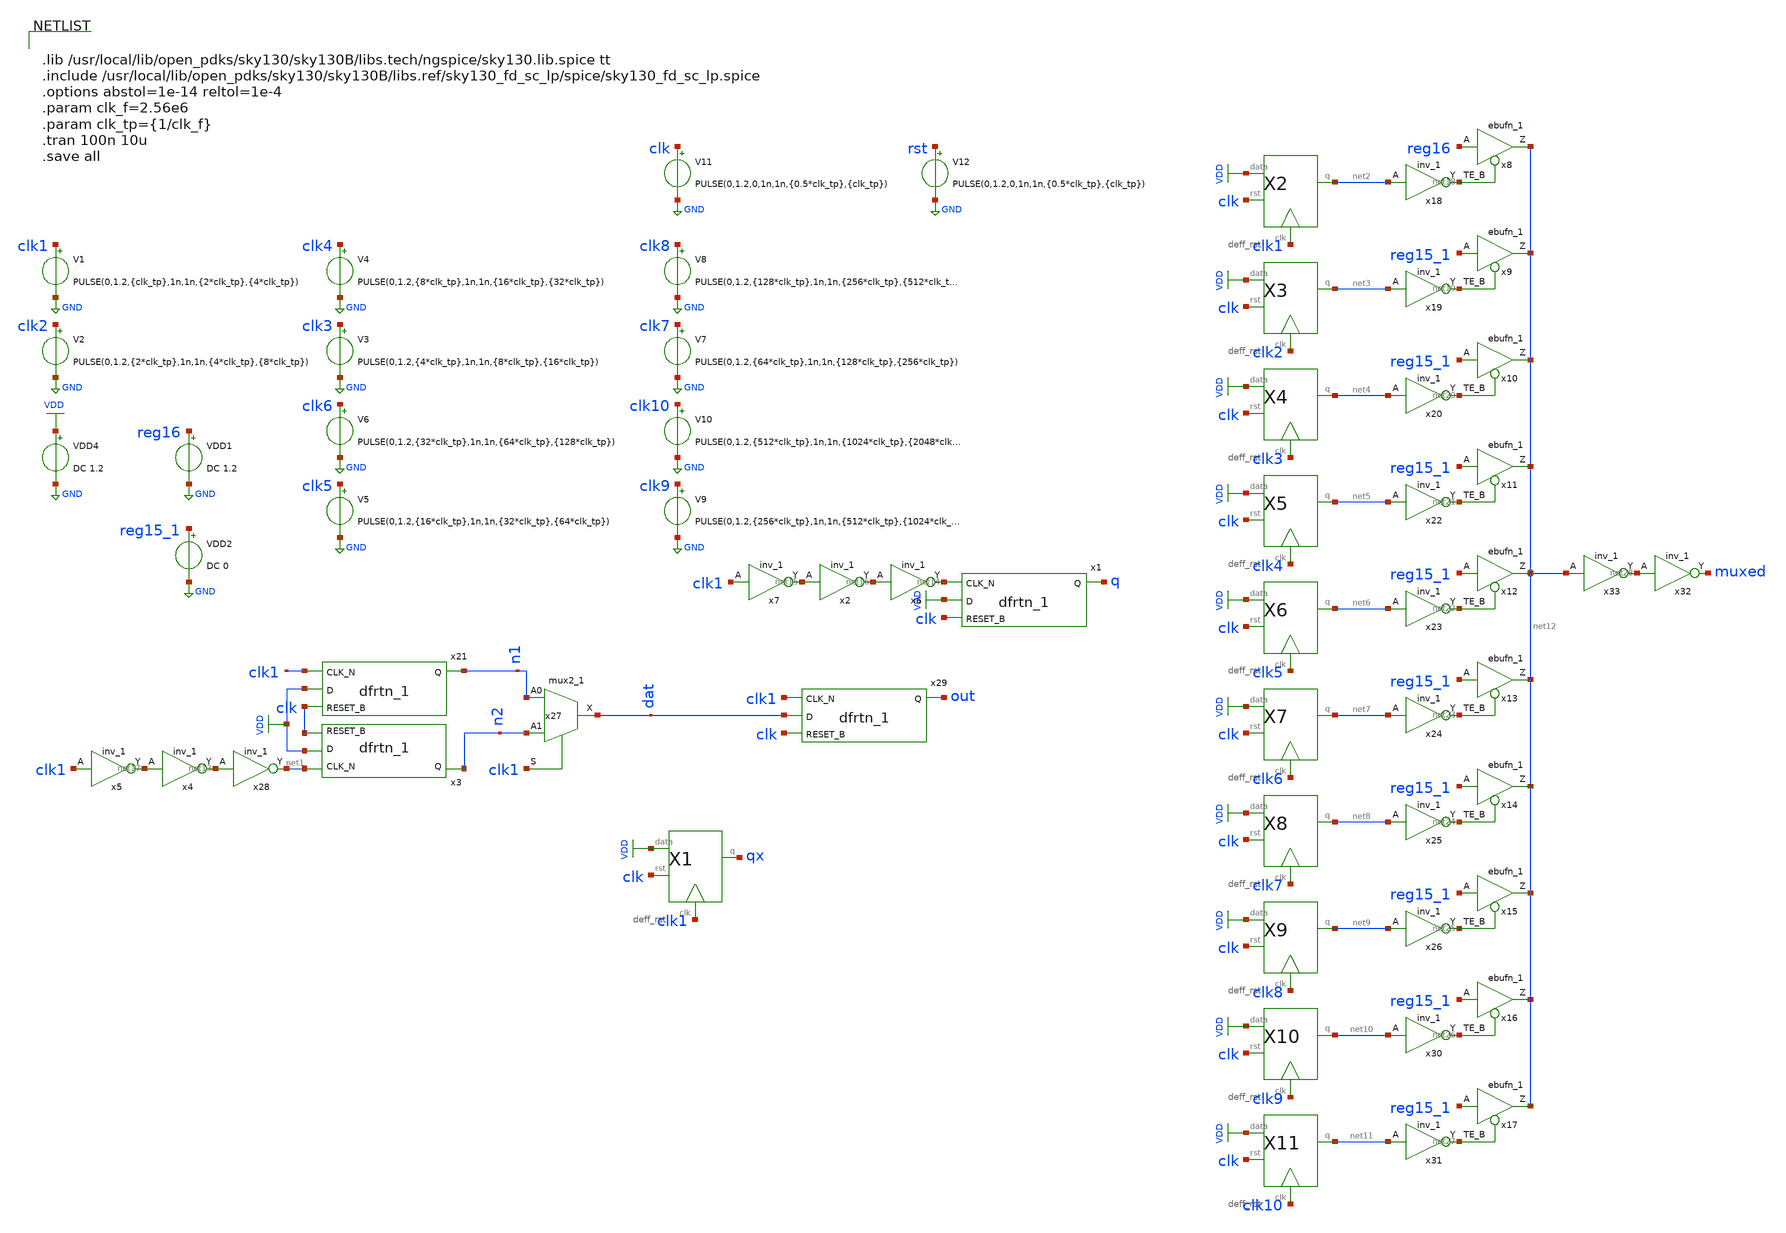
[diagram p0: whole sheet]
** sch_path: xschem/tryandtest/grayselection.sch
**.subckt grayselection
V1 clk1 GND PULSE(0,1.2,{clk_tp},1n,1n,{2*clk_tp},{4*clk_tp})
VDD4 VDD GND DC 1.2
V2 clk2 GND PULSE(0,1.2,{2*clk_tp},1n,1n,{4*clk_tp},{8*clk_tp})
V3 clk3 GND PULSE(0,1.2,{4*clk_tp},1n,1n,{8*clk_tp},{16*clk_tp})
V4 clk4 GND PULSE(0,1.2,{8*clk_tp},1n,1n,{16*clk_tp},{32*clk_tp})
V5 clk5 GND PULSE(0,1.2,{16*clk_tp},1n,1n,{32*clk_tp},{64*clk_tp})
V6 clk6 GND PULSE(0,1.2,{32*clk_tp},1n,1n,{64*clk_tp},{128*clk_tp})
V7 clk7 GND PULSE(0,1.2,{64*clk_tp},1n,1n,{128*clk_tp},{256*clk_tp})
V8 clk8 GND PULSE(0,1.2,{128*clk_tp},1n,1n,{256*clk_tp},{512*clk_tp})
V9 clk9 GND PULSE(0,1.2,{256*clk_tp},1n,1n,{512*clk_tp},{1024*clk_tp})
V10 clk10 GND PULSE(0,1.2,{512*clk_tp},1n,1n,{1024*clk_tp},{2048*clk_tp})
VDD1 reg16 GND DC 1.2
VDD2 reg15_1 GND DC 0
V11 clk GND PULSE(0,1.2,0,1n,1n,{0.5*clk_tp},{clk_tp})
x27 n1 n2 clk1 GND GND VDD VDD dat sky130_fd_sc_lp__mux2_1
x28 net13 GND GND VDD VDD net1 sky130_fd_sc_lp__inv_1
x29 clk1 dat clk GND GND VDD VDD out sky130_fd_sc_lp__dfrtn_1
x21 clk1 VDD clk GND GND VDD VDD n1 sky130_fd_sc_lp__dfrtn_1
x1 net14 VDD clk GND GND VDD VDD q sky130_fd_sc_lp__dfrtn_1
x2 net15 GND GND VDD VDD net16 sky130_fd_sc_lp__inv_1
x6 net16 GND GND VDD VDD net14 sky130_fd_sc_lp__inv_1
x7 clk1 GND GND VDD VDD net15 sky130_fd_sc_lp__inv_1
x3 net1 VDD clk GND GND VDD VDD n2 sky130_fd_sc_lp__dfrtn_1
x4 net17 GND GND VDD VDD net13 sky130_fd_sc_lp__inv_1
x5 clk1 GND GND VDD VDD net17 sky130_fd_sc_lp__inv_1
X1 VDD clk1 qx clk deff_rst
X2 VDD clk1 net2 clk deff_rst
X3 VDD clk2 net3 clk deff_rst
X4 VDD clk3 net4 clk deff_rst
X5 VDD clk4 net5 clk deff_rst
X6 VDD clk5 net6 clk deff_rst
X7 VDD clk6 net7 clk deff_rst
X8 VDD clk7 net8 clk deff_rst
X9 VDD clk8 net9 clk deff_rst
X10 VDD clk9 net10 clk deff_rst
X11 VDD clk10 net11 clk deff_rst
x8 reg16 net18 GND GND VDD VDD net12 sky130_fd_sc_lp__ebufn_1
x9 reg15_1 net19 GND GND VDD VDD net12 sky130_fd_sc_lp__ebufn_1
x10 reg15_1 net20 GND GND VDD VDD net12 sky130_fd_sc_lp__ebufn_1
x11 reg15_1 net21 GND GND VDD VDD net12 sky130_fd_sc_lp__ebufn_1
x12 reg15_1 net22 GND GND VDD VDD net12 sky130_fd_sc_lp__ebufn_1
x13 reg15_1 net23 GND GND VDD VDD net12 sky130_fd_sc_lp__ebufn_1
x14 reg15_1 net24 GND GND VDD VDD net12 sky130_fd_sc_lp__ebufn_1
x15 reg15_1 net25 GND GND VDD VDD net12 sky130_fd_sc_lp__ebufn_1
x16 reg15_1 net26 GND GND VDD VDD net12 sky130_fd_sc_lp__ebufn_1
x17 reg15_1 net27 GND GND VDD VDD net12 sky130_fd_sc_lp__ebufn_1
x18 net2 GND GND VDD VDD net18 sky130_fd_sc_lp__inv_1
x19 net3 GND GND VDD VDD net19 sky130_fd_sc_lp__inv_1
x20 net4 GND GND VDD VDD net20 sky130_fd_sc_lp__inv_1
x22 net5 GND GND VDD VDD net21 sky130_fd_sc_lp__inv_1
x23 net6 GND GND VDD VDD net22 sky130_fd_sc_lp__inv_1
x24 net7 GND GND VDD VDD net23 sky130_fd_sc_lp__inv_1
x25 net8 GND GND VDD VDD net24 sky130_fd_sc_lp__inv_1
x26 net9 GND GND VDD VDD net25 sky130_fd_sc_lp__inv_1
x30 net10 GND GND VDD VDD net26 sky130_fd_sc_lp__inv_1
x31 net11 GND GND VDD VDD net27 sky130_fd_sc_lp__inv_1
V12 rst GND PULSE(0,1.2,0,1n,1n,{0.5*clk_tp},{clk_tp})
x32 net28 GND GND VDD VDD muxed sky130_fd_sc_lp__inv_1
x33 net12 GND GND VDD VDD net28 sky130_fd_sc_lp__inv_1
**** begin user architecture code


.lib /usr/local/lib/open_pdks/sky130/sky130B/libs.tech/ngspice/sky130.lib.spice tt
.include /usr/local/lib/open_pdks/sky130/sky130B/libs.ref/sky130_fd_sc_lp/spice/sky130_fd_sc_lp.spice
.options abstol=1e-14 reltol=1e-4
.param clk_f=2.56e6
.param clk_tp={1/clk_f}
.tran 100n 10u
.save all


**** end user architecture code
**.ends

* expanding   symbol:  tryandtest/deff_rst.sym # of pins=4
** sym_path: xschem/tryandtest/deff_rst.sym
** sch_path: xschem/tryandtest/deff_rst.sch
.subckt deff_rst data clk q rst
*.ipin clk
*.ipin data
*.opin q
*.ipin rst
x3 net2 net3 clk GND GND VDD VDD q sky130_fd_sc_lp__mux2_1
x21 net1 data rst GND GND VDD VDD net2 sky130_fd_sc_lp__dfrtn_1
x2 net4 GND GND VDD VDD net1 sky130_fd_sc_lp__inv_1
x5 net5 GND GND VDD VDD net4 sky130_fd_sc_lp__inv_1
x1 net1 data rst GND GND VDD VDD net3 sky130_fd_sc_lp__dfrtp_1
x4 net6 GND GND VDD VDD net5 sky130_fd_sc_lp__inv_1
x6 clk GND GND VDD VDD net6 sky130_fd_sc_lp__inv_1
.ends

.GLOBAL GND
.GLOBAL VDD
.end
